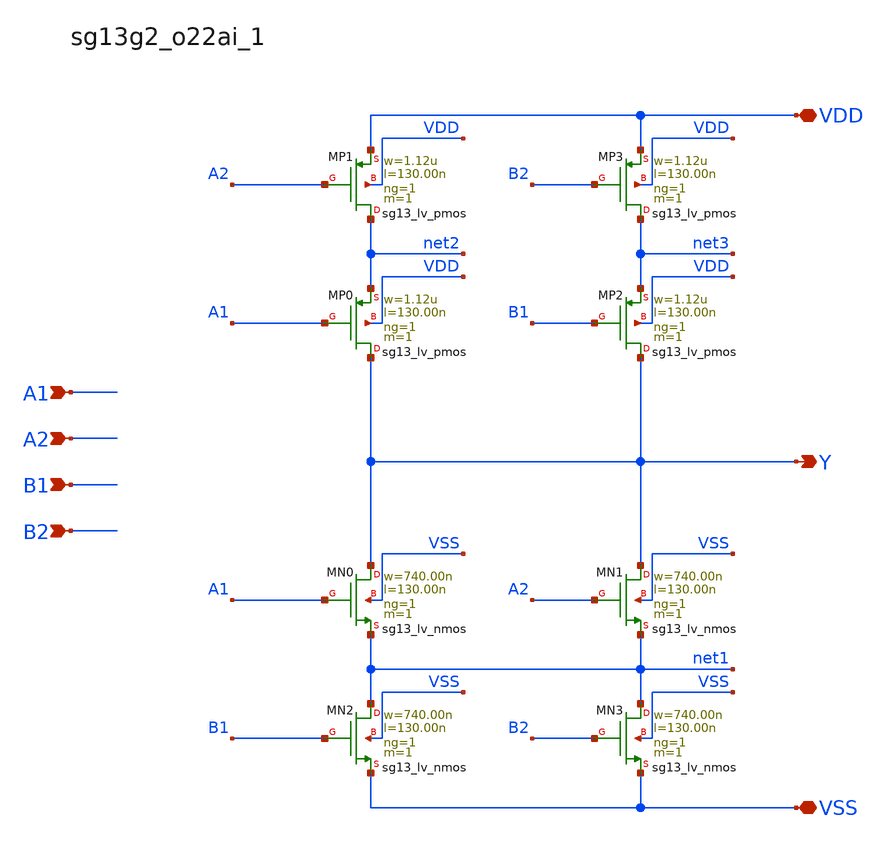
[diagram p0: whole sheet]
** sch_path: outputs/sg13g2_cells/cells/sg13g2_o22ai_1/sg13g2_o22ai_1.sch
**.subckt sg13g2_o22ai_1 Y A1 A2 B1 B2 VDD VSS
*.opin Y
*.ipin A1
*.ipin A2
*.ipin B1
*.ipin B2
*.iopin VDD
*.iopin VSS
XMN0 Y A1 net1 VSS sg13_lv_nmos w=740.00n l=130.00n ng=1 m=1 mm_ok=1
XMN1 Y A2 net1 VSS sg13_lv_nmos w=740.00n l=130.00n ng=1 m=1 mm_ok=1
XMN2 net1 B1 VSS VSS sg13_lv_nmos w=740.00n l=130.00n ng=1 m=1 mm_ok=1
XMN3 net1 B2 VSS VSS sg13_lv_nmos w=740.00n l=130.00n ng=1 m=1 mm_ok=1
XMP0 Y A1 net2 VDD sg13_lv_pmos w=1.12u l=130.00n ng=1 m=1 mm_ok=1
XMP1 net2 A2 VDD VDD sg13_lv_pmos w=1.12u l=130.00n ng=1 m=1 mm_ok=1
XMP2 Y B1 net3 VDD sg13_lv_pmos w=1.12u l=130.00n ng=1 m=1 mm_ok=1
XMP3 net3 B2 VDD VDD sg13_lv_pmos w=1.12u l=130.00n ng=1 m=1 mm_ok=1
**.ends
.end
